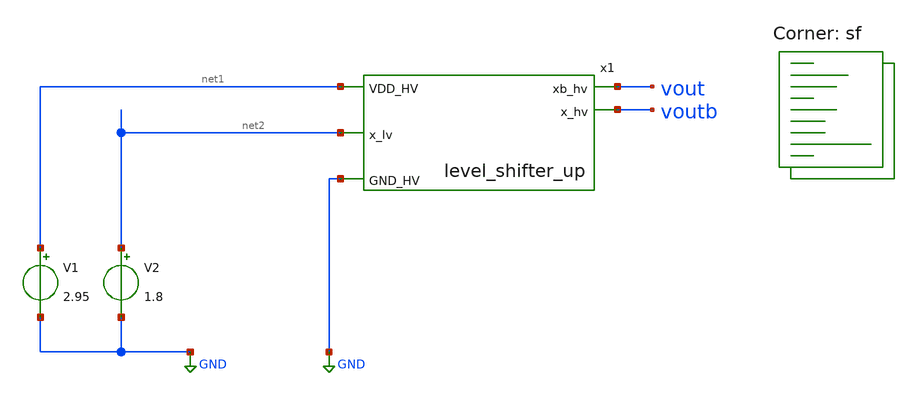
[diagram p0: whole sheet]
** sch_path: xschem/untitled.sch
**.subckt untitled
V1 net1 GND 2.95
V2 net2 GND 1.8
x1 net1 vout voutb net2 GND level_shifter_up
**** begin user architecture code


.dc v2 0 1.8 0.01
.save all
.control
foreach temp_val -40 25 85
   set temp=$temp_val
   foreach val 2.95 3.3 4.5 5.5
      alter v1 $val
      run
   end
end
plot dc1.v(vout) dc2.v(vout) dc3.v(vout) dc4.v(vout) dc5.v(vout) dc6.v(vout) dc7.v(vout) dc8.v(vout)
+ dc9.v(vout) dc10.v(vout) dc11.v(vout) dc12.v(vout)
.endc


.lib $::SKYWATER_MODELS/sky130.lib.spice sf
**** end user architecture code
**.ends

* expanding   symbol:  level_shifter_up.sym # of pins=5
** sym_path: xschem/level_shifter_up.sym
** sch_path: xschem/level_shifter_up.sch
.subckt level_shifter_up VDD_HV xb_hv x_hv x_lv GND_HV
*.ipin VDD_HV
*.ipin GND_HV
*.ipin x_lv
*.opin x_hv
*.opin xb_hv
XM65 xb_hv xbb GND_HV GND_HV sky130_fd_pr__nfet_g5v0d10v5 L=0.5 W=1 nf=1 ad='int((nf+1)/2) * W/nf * 0.29'
+ as='int((nf+2)/2) * W/nf * 0.29' pd='2*int((nf+1)/2) * (W/nf + 0.29)' ps='2*int((nf+2)/2) * (W/nf + 0.29)'
+ nrd='0.29 / W' nrs='0.29 / W' sa=0 sb=0 sd=0 mult=1 m=1
XM66 x_hv xb GND_HV GND_HV sky130_fd_pr__nfet_g5v0d10v5 L=0.5 W=1 nf=1 ad='int((nf+1)/2) * W/nf * 0.29'
+ as='int((nf+2)/2) * W/nf * 0.29' pd='2*int((nf+1)/2) * (W/nf + 0.29)' ps='2*int((nf+2)/2) * (W/nf + 0.29)'
+ nrd='0.29 / W' nrs='0.29 / W' sa=0 sb=0 sd=0 mult=1 m=1
XM67 xb_hv x_hv VDD_HV VDD_HV sky130_fd_pr__pfet_g5v0d10v5 L=0.5 W=2 nf=1 ad='int((nf+1)/2) * W/nf * 0.29'
+ as='int((nf+2)/2) * W/nf * 0.29' pd='2*int((nf+1)/2) * (W/nf + 0.29)' ps='2*int((nf+2)/2) * (W/nf + 0.29)'
+ nrd='0.29 / W' nrs='0.29 / W' sa=0 sb=0 sd=0 mult=1 m=1
XM68 x_hv xb_hv VDD_HV VDD_HV sky130_fd_pr__pfet_g5v0d10v5 L=0.5 W=2 nf=1 ad='int((nf+1)/2) * W/nf * 0.29'
+ as='int((nf+2)/2) * W/nf * 0.29' pd='2*int((nf+1)/2) * (W/nf + 0.29)' ps='2*int((nf+2)/2) * (W/nf + 0.29)'
+ nrd='0.29 / W' nrs='0.29 / W' sa=0 sb=0 sd=0 mult=1 m=1
XM1 xb x_lv GND_HV GND_HV sky130_fd_pr__nfet_g5v0d10v5 L=0.5 W=3 nf=3 ad='int((nf+1)/2) * W/nf * 0.29'
+ as='int((nf+2)/2) * W/nf * 0.29' pd='2*int((nf+1)/2) * (W/nf + 0.29)' ps='2*int((nf+2)/2) * (W/nf + 0.29)'
+ nrd='0.29 / W' nrs='0.29 / W' sa=0 sb=0 sd=0 mult=1 m=1
XM2 xbb xb GND_HV GND_HV sky130_fd_pr__nfet_g5v0d10v5 L=0.5 W=1 nf=1 ad='int((nf+1)/2) * W/nf * 0.29'
+ as='int((nf+2)/2) * W/nf * 0.29' pd='2*int((nf+1)/2) * (W/nf + 0.29)' ps='2*int((nf+2)/2) * (W/nf + 0.29)'
+ nrd='0.29 / W' nrs='0.29 / W' sa=0 sb=0 sd=0 mult=1 m=1
XM3 xb x_lv VDD_HV VDD_HV sky130_fd_pr__pfet_g5v0d10v5 L=2 W=0.5 nf=1 ad='int((nf+1)/2) * W/nf * 0.29'
+ as='int((nf+2)/2) * W/nf * 0.29' pd='2*int((nf+1)/2) * (W/nf + 0.29)' ps='2*int((nf+2)/2) * (W/nf + 0.29)'
+ nrd='0.29 / W' nrs='0.29 / W' sa=0 sb=0 sd=0 mult=1 m=1
XM4 xbb xb VDD_HV VDD_HV sky130_fd_pr__pfet_g5v0d10v5 L=0.5 W=2 nf=1 ad='int((nf+1)/2) * W/nf * 0.29'
+ as='int((nf+2)/2) * W/nf * 0.29' pd='2*int((nf+1)/2) * (W/nf + 0.29)' ps='2*int((nf+2)/2) * (W/nf + 0.29)'
+ nrd='0.29 / W' nrs='0.29 / W' sa=0 sb=0 sd=0 mult=1 m=1
.ends

.GLOBAL GND
.end
